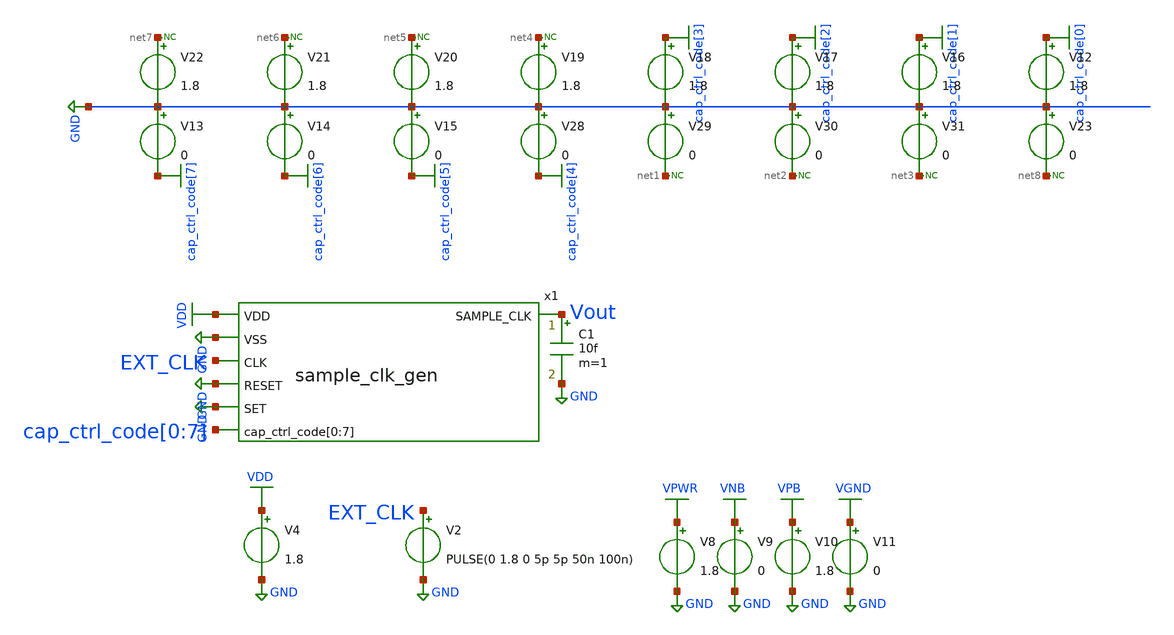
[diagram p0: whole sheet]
** sch_path: module/sar_top/sar_top/tb_sample_clk_gen.sch
**.subckt tb_sample_clk_gen
V2 EXT_CLK GND PULSE(0 1.8 0 5p 5p 50n 100n)
V4 VDD GND 1.8
x1 Vout VDD GND EXT_CLK GND GND cap_ctrl_code[0] cap_ctrl_code[1] cap_ctrl_code[2] cap_ctrl_code[3]
+ cap_ctrl_code[4] cap_ctrl_code[5] cap_ctrl_code[6] cap_ctrl_code[7] sample_clk_gen
C1 Vout GND 10f m=1
V12 cap_ctrl_code[0] GND 1.8
V13 GND cap_ctrl_code[7] 0
V14 GND cap_ctrl_code[6] 0
V15 GND cap_ctrl_code[5] 0
V28 GND cap_ctrl_code[4] 0
V29 GND net1 0
V30 GND net2 0
V31 GND net3 0
V16 cap_ctrl_code[1] GND 1.8
V17 cap_ctrl_code[2] GND 1.8
V18 cap_ctrl_code[3] GND 1.8
V19 net4 GND 1.8
V20 net5 GND 1.8
V21 net6 GND 1.8
V22 net7 GND 1.8
V23 GND net8 0
* noconn #net7
* noconn #net6
* noconn #net5
* noconn #net4
* noconn #net1
* noconn #net2
* noconn #net3
* noconn #net8
V8 VPWR GND 1.8
V9 VNB GND 0
V10 VPB GND 1.8
V11 VGND GND 0
**** begin user architecture code



.lib /foss/pdks/sky130A/libs.tech/ngspice/sky130.lib.spice tt
.include /foss/pdks/sky130A/libs.ref/sky130_fd_sc_hd/spice/sky130_fd_sc_hd.spice


.tran 1ns 200ns

.control
	option temp = 25
	let vdd_act = 1.8

	alter V4 vdd_act

	run
	plot V(Vout) V(EXT_CLK)
.endc
.save all



**** end user architecture code
**.ends
.GLOBAL GND
.GLOBAL VDD
.GLOBAL cap_ctrl_code[7]
.GLOBAL cap_ctrl_code[6]
.GLOBAL cap_ctrl_code[5]
.GLOBAL cap_ctrl_code[4]
.GLOBAL cap_ctrl_code[3]
.GLOBAL cap_ctrl_code[2]
.GLOBAL cap_ctrl_code[1]
.GLOBAL cap_ctrl_code[0]
.GLOBAL VGND
.GLOBAL VNB
.GLOBAL VPB
.GLOBAL VPWR
.end
